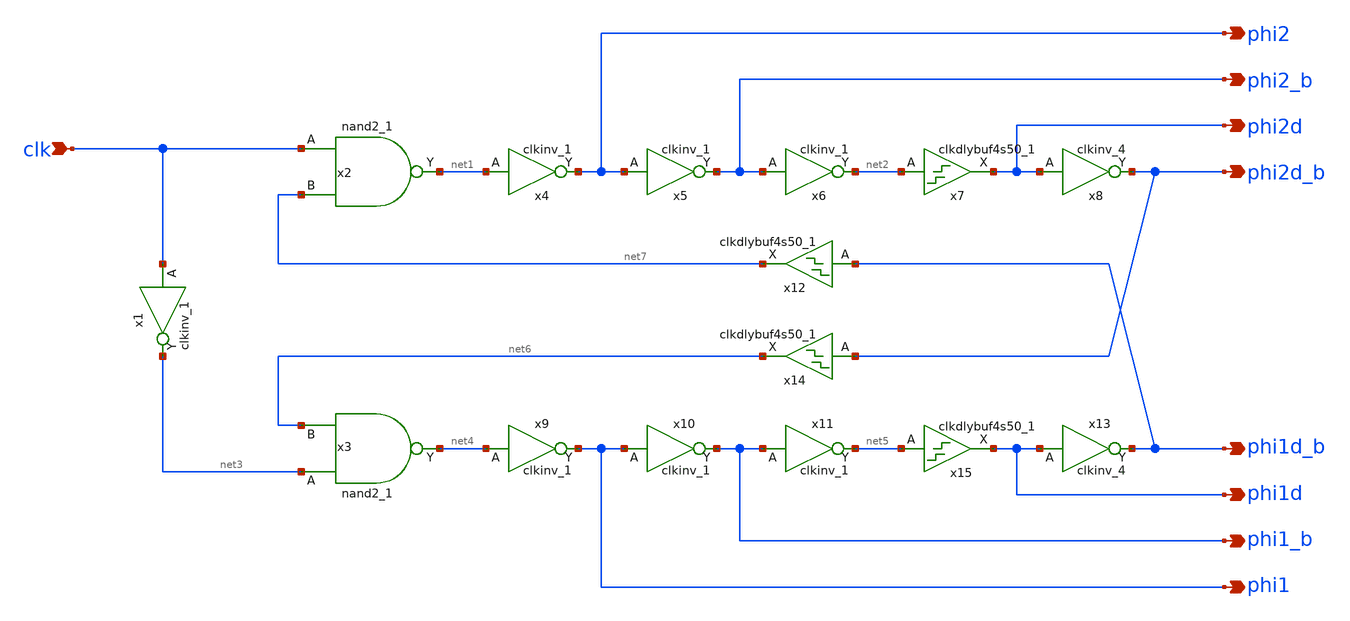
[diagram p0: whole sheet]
** sch_path: design/schematic/clock.sch
**.subckt clock clk phi2d_b phi2d phi2_b phi2 phi1d_b phi1d phi1_b phi1
*.ipin clk
*.opin phi2d_b
*.opin phi2d
*.opin phi2_b
*.opin phi2
*.opin phi1d_b
*.opin phi1d
*.opin phi1_b
*.opin phi1
x2 clk net7 GND GND VDD VDD net1 sky130_fd_sc_hd__nand2_1
x3 net3 net6 GND GND VDD VDD net4 sky130_fd_sc_hd__nand2_1
x4 net1 GND GND VDD VDD phi2 sky130_fd_sc_hd__clkinv_1
x5 phi2 GND GND VDD VDD phi2_b sky130_fd_sc_hd__clkinv_1
x6 phi2_b GND GND VDD VDD net2 sky130_fd_sc_hd__clkinv_1
x8 phi2d GND GND VDD VDD phi2d_b sky130_fd_sc_hd__clkinv_4
x9 net4 GND GND VDD VDD phi1 sky130_fd_sc_hd__clkinv_1
x10 phi1 GND GND VDD VDD phi1_b sky130_fd_sc_hd__clkinv_1
x11 phi1_b GND GND VDD VDD net5 sky130_fd_sc_hd__clkinv_1
x13 phi1d GND GND VDD VDD phi1d_b sky130_fd_sc_hd__clkinv_4
x1 clk GND GND VDD VDD net3 sky130_fd_sc_hd__clkinv_1
x7 net2 GND GND VDD VDD phi2d sky130_fd_sc_hd__clkdlybuf4s50_1
x12 phi1d_b GND GND VDD VDD net7 sky130_fd_sc_hd__clkdlybuf4s50_1
x14 phi2d_b GND GND VDD VDD net6 sky130_fd_sc_hd__clkdlybuf4s50_1
x15 net5 GND GND VDD VDD phi1d sky130_fd_sc_hd__clkdlybuf4s50_1
**.ends
.end
